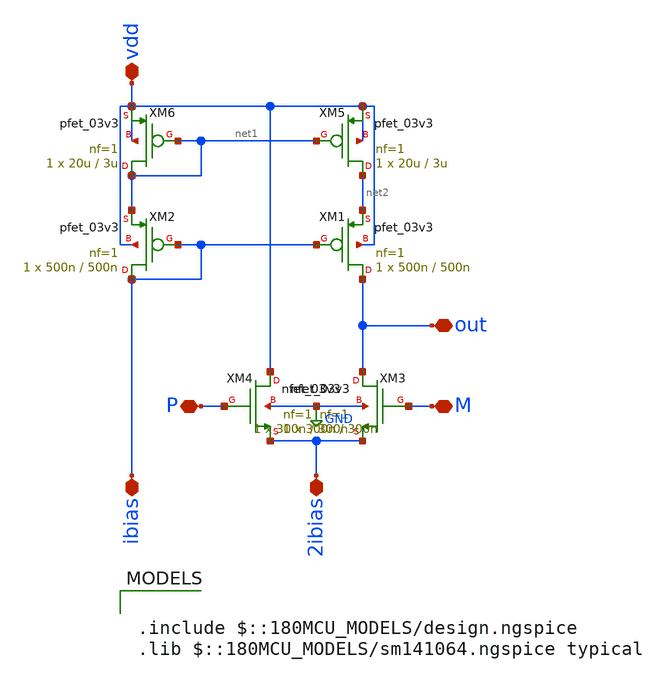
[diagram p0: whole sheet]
** sch_path: Clock_Reference/clockGenerator/clockGenerator/clockGenerator/VCIS.sch
**.subckt VCIS 2ibias ibias P M out vdd
*.iopin 2ibias
*.iopin ibias
*.iopin P
*.iopin M
*.iopin out
*.iopin vdd
XM1 out ibias net2 vdd pfet_03v3 L=500n W=500n nf=1 ad='int((nf+1)/2) * W/nf * 0.18u' as='int((nf+2)/2) * W/nf * 0.18u'
+ pd='2*int((nf+1)/2) * (W/nf + 0.18u)' ps='2*int((nf+2)/2) * (W/nf + 0.18u)' nrd='0.18u / W' nrs='0.18u / W'
+ sa=0 sb=0 sd=0 m=1
XM2 ibias ibias net1 vdd pfet_03v3 L=500n W=500n nf=1 ad='int((nf+1)/2) * W/nf * 0.18u' as='int((nf+2)/2) * W/nf * 0.18u'
+ pd='2*int((nf+1)/2) * (W/nf + 0.18u)' ps='2*int((nf+2)/2) * (W/nf + 0.18u)' nrd='0.18u / W' nrs='0.18u / W'
+ sa=0 sb=0 sd=0 m=1
XM3 out M 2ibias GND nfet_03v3 L=300n W=300n nf=1 ad='int((nf+1)/2) * W/nf * 0.18u' as='int((nf+2)/2) * W/nf * 0.18u'
+ pd='2*int((nf+1)/2) * (W/nf + 0.18u)' ps='2*int((nf+2)/2) * (W/nf + 0.18u)' nrd='0.18u / W' nrs='0.18u / W'
+ sa=0 sb=0 sd=0 m=1
XM4 vdd P 2ibias GND nfet_03v3 L=300n W=300n nf=1 ad='int((nf+1)/2) * W/nf * 0.18u' as='int((nf+2)/2) * W/nf * 0.18u'
+ pd='2*int((nf+1)/2) * (W/nf + 0.18u)' ps='2*int((nf+2)/2) * (W/nf + 0.18u)' nrd='0.18u / W' nrs='0.18u / W'
+ sa=0 sb=0 sd=0 m=1
XM5 net2 net1 vdd vdd pfet_03v3 L=3u W=20u nf=1 ad='int((nf+1)/2) * W/nf * 0.18u' as='int((nf+2)/2) * W/nf * 0.18u'
+ pd='2*int((nf+1)/2) * (W/nf + 0.18u)' ps='2*int((nf+2)/2) * (W/nf + 0.18u)' nrd='0.18u / W' nrs='0.18u / W'
+ sa=0 sb=0 sd=0 m=1
XM6 net1 net1 vdd vdd pfet_03v3 L=3u W=20u nf=1 ad='int((nf+1)/2) * W/nf * 0.18u' as='int((nf+2)/2) * W/nf * 0.18u'
+ pd='2*int((nf+1)/2) * (W/nf + 0.18u)' ps='2*int((nf+2)/2) * (W/nf + 0.18u)' nrd='0.18u / W' nrs='0.18u / W'
+ sa=0 sb=0 sd=0 m=1
**** begin user architecture code

.include $::180MCU_MODELS/design.ngspice
.lib $::180MCU_MODELS/sm141064.ngspice typical

**** end user architecture code
**.ends
.GLOBAL GND
.end
